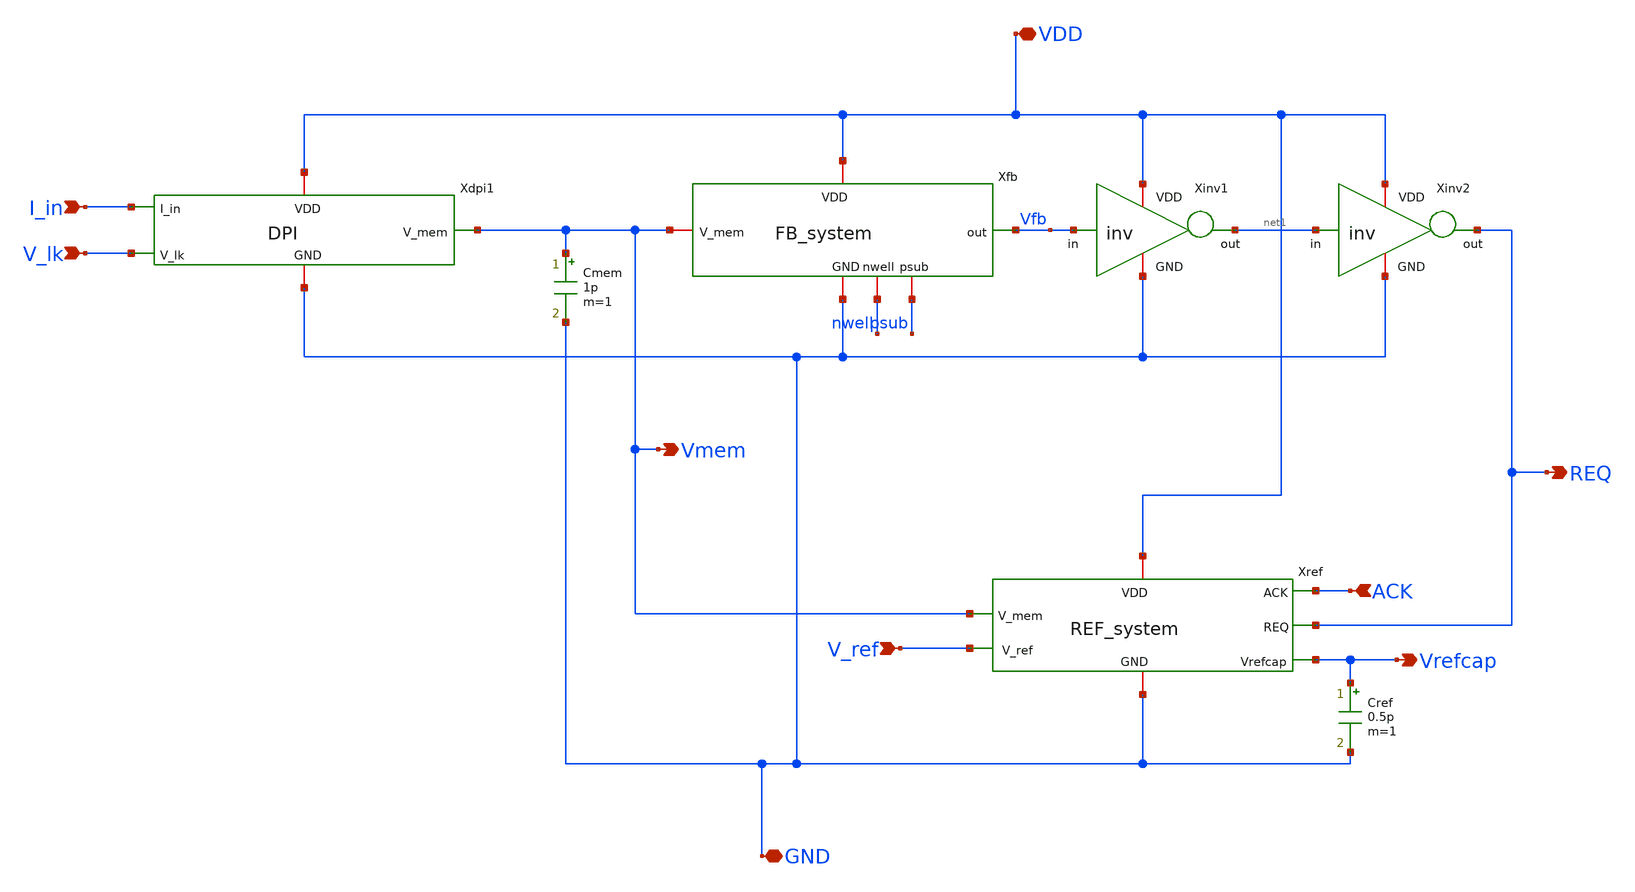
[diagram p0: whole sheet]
** sch_path: xschem/neuron_noahp.sch
**.subckt neuron_noahp V_ref GND VDD REQ ACK I_in V_lk Vmem Vrefcap
*.ipin V_ref
*.iopin GND
*.iopin VDD
*.opin REQ
*.ipin ACK
*.ipin I_in
*.ipin V_lk
*.opin Vmem
*.opin Vrefcap
Xinv1 VDD Vfb net1 GND inv
Xinv2 VDD net1 REQ GND inv
Xdpi1 I_in VDD Vmem V_lk GND DPI
Xfb VDD Vfb Vmem GND nwell psub FB_system
Xref VDD ACK Vmem REQ Vrefcap GND V_ref REF_system
Cmem Vmem GND 1p m=1
Cref Vrefcap GND 0.5p m=1
**.ends

* expanding   symbol:  inv.sym # of pins=4
** sym_path: xschem/inv.sym
** sch_path: xschem/inv.sch
.subckt inv VDD in out GND
*.ipin in
*.iopin VDD
*.iopin GND
*.opin out
XM1 out in VDD nwell sg13_hv_pmos w=4u l=0.5u ng=1 m=1 mm_ok=1
XM2 out in GND psub sg13_hv_nmos w=4u l=0.5u ng=1 m=1 mm_ok=1
XR1 GND psub ptap1 R=95.61 w=2.75e-6 l=1e-6
XR2 VDD nwell ntap1 R=95.61 w=2.75e-6 l=1e-6
.ends


* expanding   symbol:  DPI.sym # of pins=5
** sym_path: DPI.sym
** sch_path: DPI.sch
.subckt DPI I_in VDD V_mem V_lk GND
*.opin V_mem
*.ipin V_lk
*.ipin I_in
*.iopin VDD
*.iopin GND
XMdifl GND V_lk I_in VDD sg13_hv_pmos w=2u l=2u ng=2 m=8 mm_ok=1
XMdifr V_mem V_mem I_in VDD sg13_hv_pmos w=2u l=2u ng=2 m=8 mm_ok=1
XMtau V_mem V_lk GND GND sg13_hv_nmos w=4u l=4u ng=2 m=4 mm_ok=1
.ends


* expanding   symbol:  FB_system.sym # of pins=6
** sym_path: xschem/FB_system.sym
** sch_path: xschem/FB_system.sch
.subckt FB_system VDD out V_mem GND nwell psub
*.opin out
*.iopin V_mem
*.iopin VDD
*.iopin GND
*.iopin nwell
*.iopin psub
XMmirr Vmir Vmir VDD nwell sg13_hv_pmos w=4u l=2u ng=4 m=1 mm_ok=1
XMmirl4 V_mem Vmir net1 nwell sg13_hv_pmos w=1u l=2u ng=1 m=1 mm_ok=1
XMthr out V_mem Vmir nwell sg13_hv_pmos w=4u l=2u ng=4 m=1 mm_ok=1
XMmem1 out V_mem net2 psub sg13_hv_nmos w=1u l=2u ng=1 m=2 mm_ok=1
XMmirl3 net1 Vmir net3 nwell sg13_hv_pmos w=1u l=2u ng=1 m=1 mm_ok=1
XMmirl2 net3 Vmir net4 nwell sg13_hv_pmos w=1u l=2u ng=1 m=1 mm_ok=1
XMmirl1 net4 Vmir VDD nwell sg13_hv_pmos w=1u l=2u ng=1 m=1 mm_ok=1
XMmem2 net2 V_mem net5 psub sg13_hv_nmos w=1u l=2u ng=1 m=2 mm_ok=1
XMmem3 net5 V_mem net6 psub sg13_hv_nmos w=1u l=2u ng=1 m=2 mm_ok=1
XMmem4 net6 V_mem GND psub sg13_hv_nmos w=1u l=2u ng=1 m=2 mm_ok=1
XMdum1 GND GND GND psub sg13_hv_nmos w=6u l=2u ng=6 m=2 mm_ok=1
XMdum2 GND GND GND psub sg13_hv_nmos w=1u l=2u ng=1 m=2 mm_ok=1
XMdum3 out GND GND psub sg13_hv_nmos w=1u l=2u ng=1 m=2 mm_ok=1
XMdum4 VDD VDD VDD nwell sg13_hv_pmos w=6u l=2u ng=6 m=2 mm_ok=1
XMdum5 VDD VDD VDD nwell sg13_hv_pmos w=1u l=2u ng=1 m=3 mm_ok=1
XMdum6 out VDD VDD nwell sg13_hv_pmos w=1u l=2u ng=1 m=2 mm_ok=1
XMdum7 V_mem VDD VDD nwell sg13_hv_pmos w=1u l=2u ng=1 m=1 mm_ok=1
.ends


* expanding   symbol:  REF_system.sym # of pins=7
** sym_path: xschem/REF_system.sym
** sch_path: xschem/REF_system.sch
.subckt REF_system VDD ACK V_mem REQ Vrefcap GND V_ref
*.iopin VDD
*.iopin GND
*.ipin V_ref
*.ipin REQ
*.ipin ACK
*.ipin V_mem
*.opin Vrefcap
XM10 Vrefcap REQ net2 VDD sg13_hv_pmos w=1u l=0.5u ng=1 m=1 mm_ok=1
XM11 Vrefcap REQ net1 GND sg13_hv_nmos w=1u l=0.5u ng=1 m=1 mm_ok=1
XM12 net2 ACK VDD VDD sg13_hv_pmos w=1u l=0.5u ng=1 m=1 mm_ok=1
XM13 V_mem Vrefcap GND GND sg13_hv_nmos w=1u l=0.5u ng=1 m=1 mm_ok=1
XM14 net1 V_ref GND GND sg13_hv_nmos w=4u l=4u ng=2 m=4 mm_ok=1
.ends

.end
